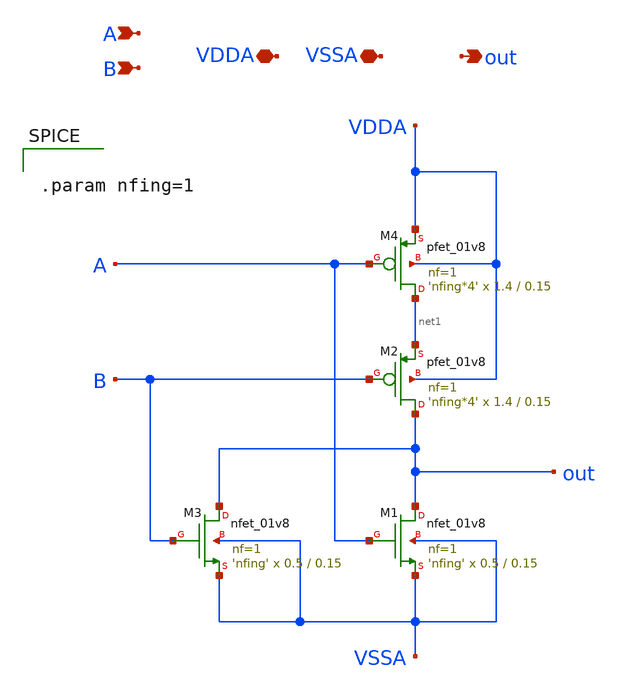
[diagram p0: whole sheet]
** sch_path: Xschem/sky130A/gate_nor_xn.sch
**.subckt gate_nor_xn A VDDA VSSA out B
*.ipin A
*.iopin VDDA
*.iopin VSSA
*.opin out
*.ipin B
XM1 out A VSSA VSSA sky130_fd_pr__nfet_01v8 L=0.15 W=0.5 nf=1 ad='int((1 + 1)/2) * 0.5 / 1 * 0.29' as='int((1 + 2)/2) * 0.5 / 1 * 0.29'
+ pd='2*int((1 + 1)/2) * (0.5 / 1 + 0.29)' ps='2*int((1 + 2)/2) * (0.5 / 1 + 0.29)' nrd='0.29 / 0.5 ' nrs='0.29 / 0.5 '
+ sa=0 sb=0 sd=0 mult='nfing' m='nfing'
XM2 out B net1 VDDA sky130_fd_pr__pfet_01v8 L=0.15 W=1.4 nf=1 ad='int((1 + 1)/2) * 1.4 / 1 * 0.29' as='int((1 + 2)/2) * 1.4 / 1 * 0.29'
+ pd='2*int((1 + 1)/2) * (1.4 / 1 + 0.29)' ps='2*int((1 + 2)/2) * (1.4 / 1 + 0.29)' nrd='0.29 / 1.4 ' nrs='0.29 / 1.4 '
+ sa=0 sb=0 sd=0 mult='nfing*4' m='nfing*4'
XM3 out B VSSA VSSA sky130_fd_pr__nfet_01v8 L=0.15 W=0.5 nf=1 ad='int((1 + 1)/2) * 0.5 / 1 * 0.29' as='int((1 + 2)/2) * 0.5 / 1 * 0.29'
+ pd='2*int((1 + 1)/2) * (0.5 / 1 + 0.29)' ps='2*int((1 + 2)/2) * (0.5 / 1 + 0.29)' nrd='0.29 / 0.5 ' nrs='0.29 / 0.5 '
+ sa=0 sb=0 sd=0 mult='nfing' m='nfing'
XM4 net1 A VDDA VDDA sky130_fd_pr__pfet_01v8 L=0.15 W=1.4 nf=1 ad='int((1 + 1)/2) * 1.4 / 1 * 0.29' as='int((1 + 2)/2) * 1.4 / 1 * 0.29'
+ pd='2*int((1 + 1)/2) * (1.4 / 1 + 0.29)' ps='2*int((1 + 2)/2) * (1.4 / 1 + 0.29)' nrd='0.29 / 1.4 ' nrs='0.29 / 1.4 '
+ sa=0 sb=0 sd=0 mult='nfing*4' m='nfing*4'
**** begin user architecture code


.param nfing=1


**** end user architecture code
**.ends
.end
